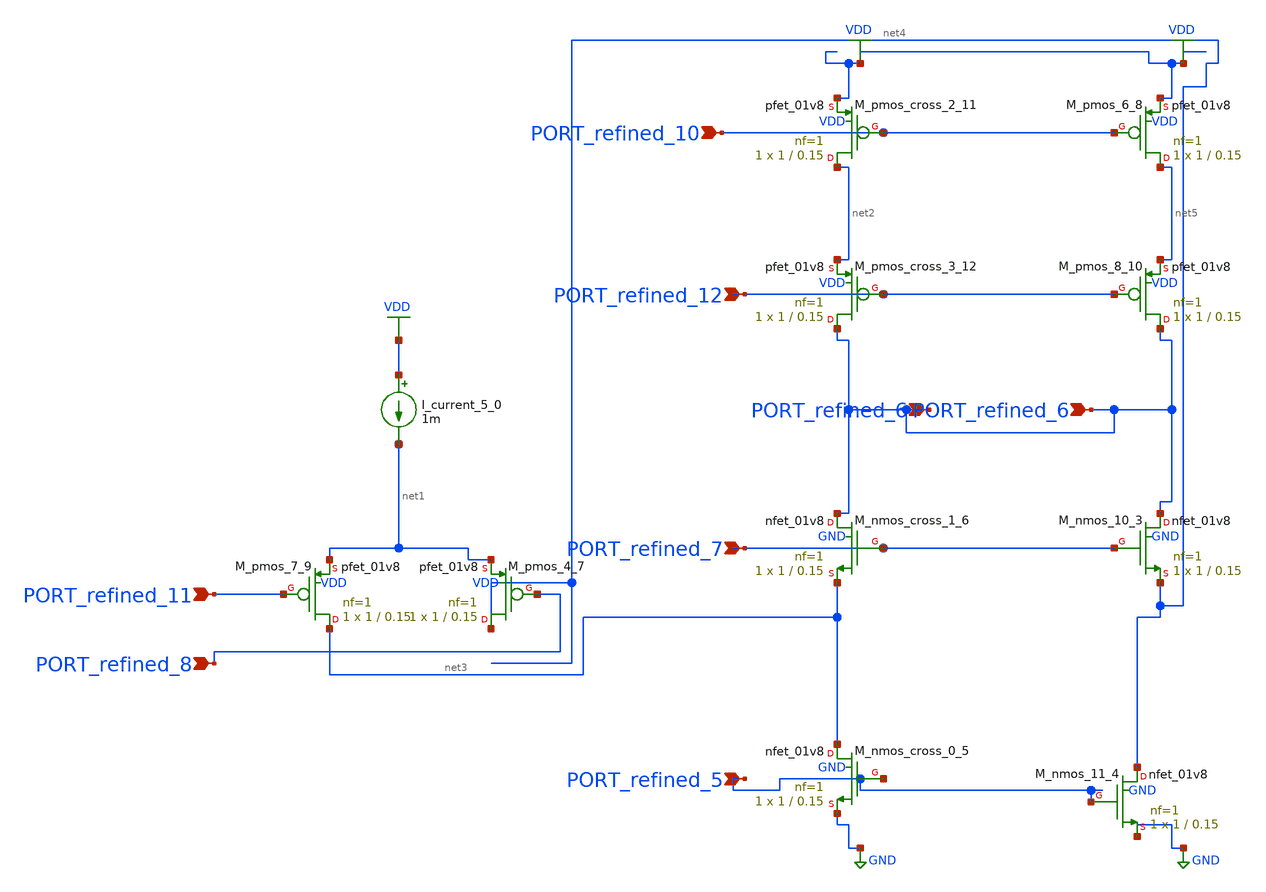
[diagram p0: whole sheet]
** sch_path: schematics/SchemGen/10_11648_j_ajpa_20241201_12_03_002.sch
**.subckt 10_11648_j_ajpa_20241201_12_03_002 PORT_refined_7 PORT_refined_12 PORT_refined_5
*+ PORT_refined_10 PORT_refined_11 PORT_refined_6 PORT_refined_8 PORT_refined_6
*.ipin PORT_refined_7
*.ipin PORT_refined_12
*.ipin PORT_refined_5
*.ipin PORT_refined_10
*.ipin PORT_refined_11
*.ipin PORT_refined_6
*.ipin PORT_refined_8
*.ipin PORT_refined_6
I_current_5_0 VDD net1 1m
XM_nmos_10_3 PORT_refined_6 PORT_refined_7 net4 GND sky130_fd_pr__nfet_01v8 L=0.15 W=1 nf=1 ad='int((1 + 1)/2) * 1 / 1 * 0.29'
+ as='int((1 + 2)/2) * 1 / 1 * 0.29' pd='2*int((1 + 1)/2) * (1 / 1 + 0.29)' ps='2*int((1 + 2)/2) * (1 / 1 + 0.29)'
+ nrd='0.29 / 1 ' nrs='0.29 / 1 ' sa=0 sb=0 sd=0 mult=1 m=1
XM_nmos_11_4 net4 PORT_refined_5 GND GND sky130_fd_pr__nfet_01v8 L=0.15 W=1 nf=1 ad='int((1 + 1)/2) * 1 / 1 * 0.29'
+ as='int((1 + 2)/2) * 1 / 1 * 0.29' pd='2*int((1 + 1)/2) * (1 / 1 + 0.29)' ps='2*int((1 + 2)/2) * (1 / 1 + 0.29)'
+ nrd='0.29 / 1 ' nrs='0.29 / 1 ' sa=0 sb=0 sd=0 mult=1 m=1
XM_nmos_cross_0_5 net3 PORT_refined_5 GND GND sky130_fd_pr__nfet_01v8 L=0.15 W=1 nf=1 ad='int((1 + 1)/2) * 1 / 1 * 0.29'
+ as='int((1 + 2)/2) * 1 / 1 * 0.29' pd='2*int((1 + 1)/2) * (1 / 1 + 0.29)' ps='2*int((1 + 2)/2) * (1 / 1 + 0.29)'
+ nrd='0.29 / 1 ' nrs='0.29 / 1 ' sa=0 sb=0 sd=0 mult=1 m=1
XM_nmos_cross_1_6 PORT_refined_6 PORT_refined_7 net3 GND sky130_fd_pr__nfet_01v8 L=0.15 W=1 nf=1 ad='int((1 + 1)/2) * 1 / 1 * 0.29'
+ as='int((1 + 2)/2) * 1 / 1 * 0.29' pd='2*int((1 + 1)/2) * (1 / 1 + 0.29)' ps='2*int((1 + 2)/2) * (1 / 1 + 0.29)'
+ nrd='0.29 / 1 ' nrs='0.29 / 1 ' sa=0 sb=0 sd=0 mult=1 m=1
XM_pmos_4_7 net4 PORT_refined_8 net1 VDD sky130_fd_pr__pfet_01v8 L=0.15 W=1 nf=1 ad='int((1 + 1)/2) * 1 / 1 * 0.29'
+ as='int((1 + 2)/2) * 1 / 1 * 0.29' pd='2*int((1 + 1)/2) * (1 / 1 + 0.29)' ps='2*int((1 + 2)/2) * (1 / 1 + 0.29)'
+ nrd='0.29 / 1 ' nrs='0.29 / 1 ' sa=0 sb=0 sd=0 mult=1 m=1
XM_pmos_6_8 net5 PORT_refined_10 VDD VDD sky130_fd_pr__pfet_01v8 L=0.15 W=1 nf=1 ad='int((1 + 1)/2) * 1 / 1 * 0.29'
+ as='int((1 + 2)/2) * 1 / 1 * 0.29' pd='2*int((1 + 1)/2) * (1 / 1 + 0.29)' ps='2*int((1 + 2)/2) * (1 / 1 + 0.29)'
+ nrd='0.29 / 1 ' nrs='0.29 / 1 ' sa=0 sb=0 sd=0 mult=1 m=1
XM_pmos_7_9 net3 PORT_refined_11 net1 VDD sky130_fd_pr__pfet_01v8 L=0.15 W=1 nf=1 ad='int((1 + 1)/2) * 1 / 1 * 0.29'
+ as='int((1 + 2)/2) * 1 / 1 * 0.29' pd='2*int((1 + 1)/2) * (1 / 1 + 0.29)' ps='2*int((1 + 2)/2) * (1 / 1 + 0.29)'
+ nrd='0.29 / 1 ' nrs='0.29 / 1 ' sa=0 sb=0 sd=0 mult=1 m=1
XM_pmos_8_10 PORT_refined_6 PORT_refined_12 net5 VDD sky130_fd_pr__pfet_01v8 L=0.15 W=1 nf=1 ad='int((1 + 1)/2) * 1 / 1 * 0.29'
+ as='int((1 + 2)/2) * 1 / 1 * 0.29' pd='2*int((1 + 1)/2) * (1 / 1 + 0.29)' ps='2*int((1 + 2)/2) * (1 / 1 + 0.29)'
+ nrd='0.29 / 1 ' nrs='0.29 / 1 ' sa=0 sb=0 sd=0 mult=1 m=1
XM_pmos_cross_2_11 net2 PORT_refined_10 VDD VDD sky130_fd_pr__pfet_01v8 L=0.15 W=1 nf=1 ad='int((1 + 1)/2) * 1 / 1 * 0.29'
+ as='int((1 + 2)/2) * 1 / 1 * 0.29' pd='2*int((1 + 1)/2) * (1 / 1 + 0.29)' ps='2*int((1 + 2)/2) * (1 / 1 + 0.29)'
+ nrd='0.29 / 1 ' nrs='0.29 / 1 ' sa=0 sb=0 sd=0 mult=1 m=1
XM_pmos_cross_3_12 PORT_refined_6 PORT_refined_12 net2 VDD sky130_fd_pr__pfet_01v8 L=0.15 W=1 nf=1 ad='int((1 + 1)/2) * 1 / 1 * 0.29'
+ as='int((1 + 2)/2) * 1 / 1 * 0.29' pd='2*int((1 + 1)/2) * (1 / 1 + 0.29)' ps='2*int((1 + 2)/2) * (1 / 1 + 0.29)'
+ nrd='0.29 / 1 ' nrs='0.29 / 1 ' sa=0 sb=0 sd=0 mult=1 m=1
**.ends
.GLOBAL GND
.GLOBAL VDD
.end
